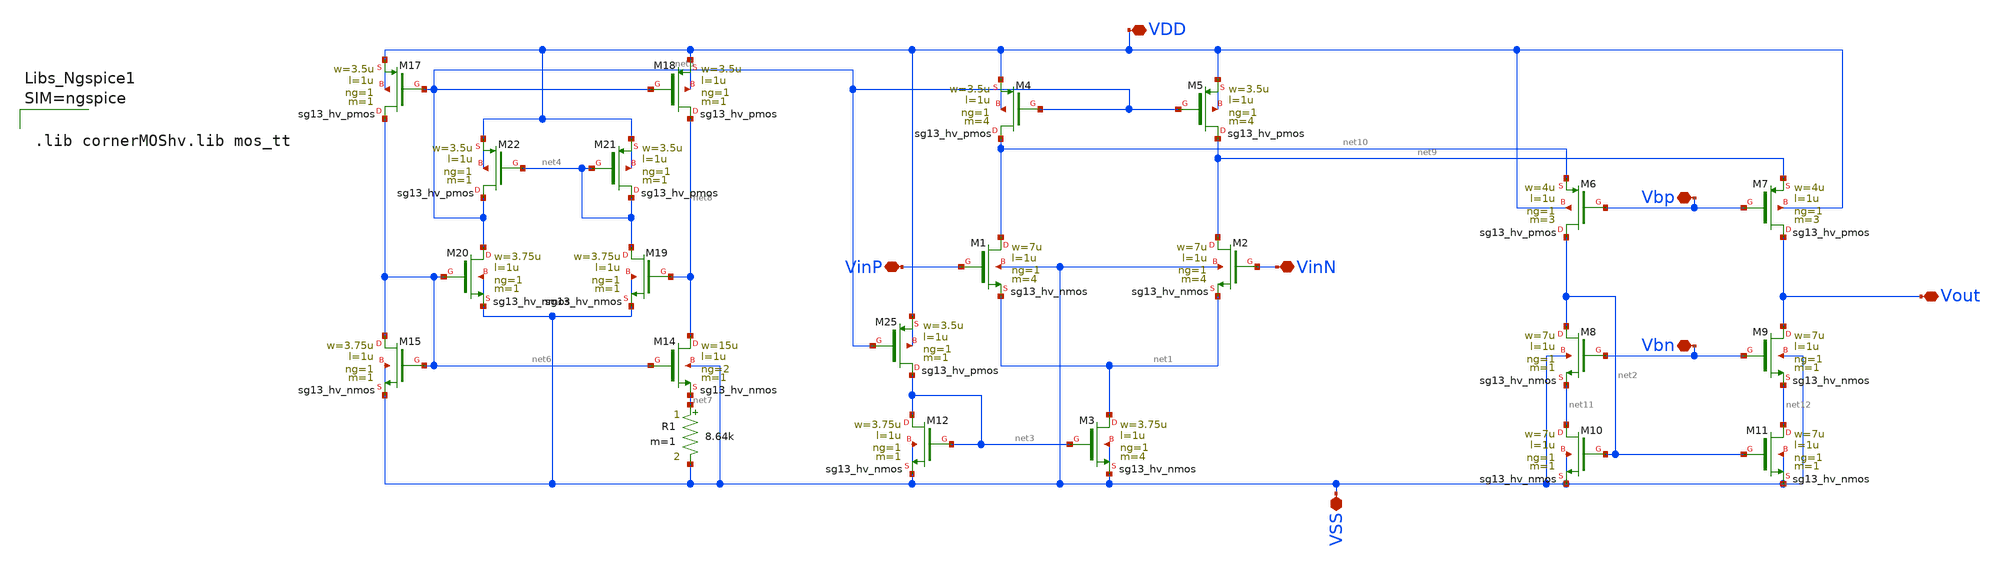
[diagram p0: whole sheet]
** sch_path: v2_bmr_bias/symbol.sch
**.subckt symbol Vbn Vbp VinP VinN Vout VDD VSS
*.iopin Vbn
*.iopin Vbp
*.iopin VinP
*.iopin VinN
*.iopin Vout
*.iopin VDD
*.iopin VSS
XM1 net10 VinP net1 VSS sg13_hv_nmos w=7u l=1u ng=1 m=4 mm_ok=1
XM2 net9 VinN net1 VSS sg13_hv_nmos w=7u l=1u ng=1 m=4 mm_ok=1
XM3 net1 net3 VSS VSS sg13_hv_nmos w=3.75u l=1u ng=1 m=4 mm_ok=1
XM4 net10 net5 VDD VDD sg13_hv_pmos w=3.5u l=1u ng=1 m=4 mm_ok=1
XM5 net9 net5 VDD VDD sg13_hv_pmos w=3.5u l=1u ng=1 m=4 mm_ok=1
XM6 net2 Vbp net10 VDD sg13_hv_pmos w=4u l=1u ng=1 m=3 mm_ok=1
XM7 Vout Vbp net9 VDD sg13_hv_pmos w=4u l=1u ng=1 m=3 mm_ok=1
XM8 net2 Vbn net11 VSS sg13_hv_nmos w=7u l=1u ng=1 m=1 mm_ok=1
XM9 Vout Vbn net12 VSS sg13_hv_nmos w=7u l=1u ng=1 m=1 mm_ok=1
XM10 net11 net2 VSS VSS sg13_hv_nmos w=7u l=1u ng=1 m=1 mm_ok=1
XM11 net12 net2 VSS VSS sg13_hv_nmos w=7u l=1u ng=1 m=1 mm_ok=1
XM25 net3 net5 VDD VDD sg13_hv_pmos w=3.5u l=1u ng=1 m=1 mm_ok=1
XM12 net3 net3 VSS VSS sg13_hv_nmos w=3.75u l=1u ng=1 m=1 mm_ok=1
R1 net7 VSS 8.64k m=1
XM14 net8 net6 net7 VSS sg13_hv_nmos w=15u l=1u ng=2 m=1 mm_ok=1
XM15 net6 net6 VSS VSS sg13_hv_nmos w=3.75u l=1u ng=1 m=1 mm_ok=1
XM17 net6 net5 VDD VDD sg13_hv_pmos w=3.5u l=1u ng=1 m=1 mm_ok=1
XM18 net8 net5 VDD VDD sg13_hv_pmos w=3.5u l=1u ng=1 m=1 mm_ok=1
XM19 net4 net8 VSS VSS sg13_hv_nmos w=3.75u l=1u ng=1 m=1 mm_ok=1
XM20 net5 net6 VSS VSS sg13_hv_nmos w=3.75u l=1u ng=1 m=1 mm_ok=1
XM21 net4 net4 VDD VDD sg13_hv_pmos w=3.5u l=1u ng=1 m=1 mm_ok=1
XM22 net5 net4 VDD VDD sg13_hv_pmos w=3.5u l=1u ng=1 m=1 mm_ok=1
**** begin user architecture code



.lib cornerMOShv.lib mos_tt



**** end user architecture code
**.ends
.end
